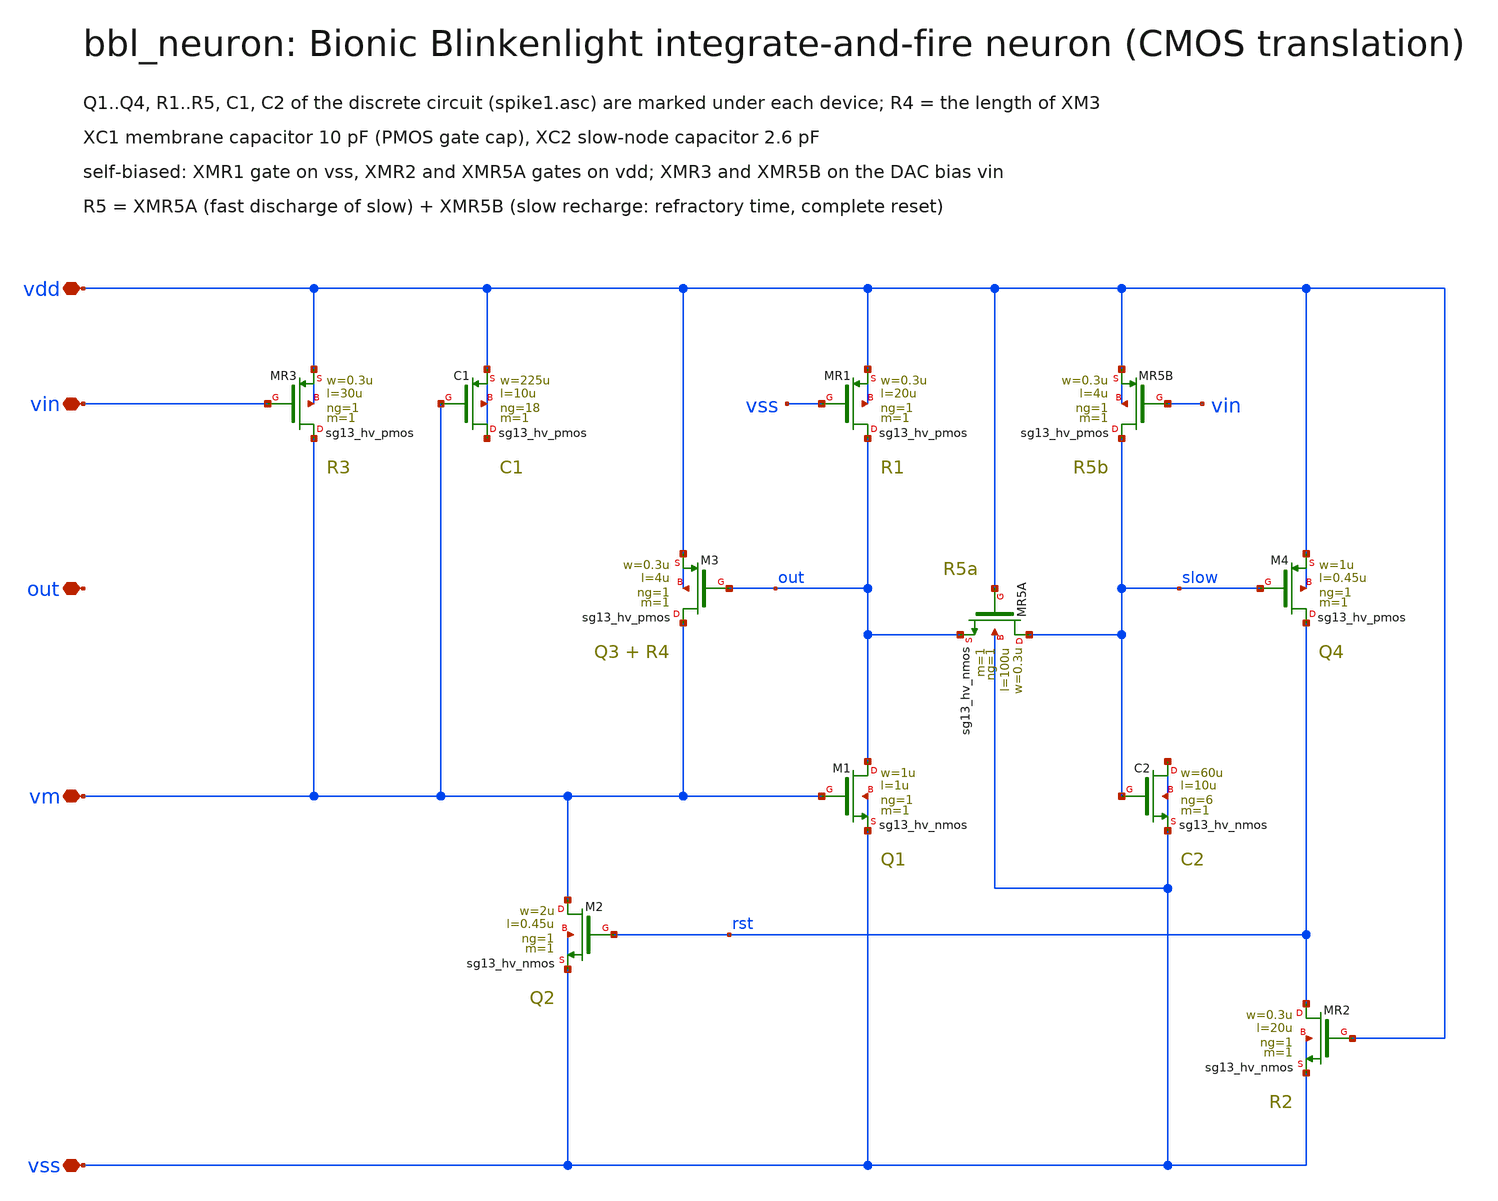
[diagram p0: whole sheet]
** sch_path: schematic/xschem/bbl_neuron.sch
**.subckt bbl_neuron vdd vss vm out vin
*.iopin vdd
*.iopin vss
*.iopin vm
*.iopin out
*.iopin vin
XMR3 vm vin vdd vdd sg13_hv_pmos w=0.3u l=30u ng=1 m=1 mm_ok=1
XC1 vdd vm vdd vdd sg13_hv_pmos w=225u l=10u ng=18 m=1 mm_ok=1
XM2 vm rst vss vss sg13_hv_nmos w=2u l=0.45u ng=1 m=1 mm_ok=1
XM3 vm out vdd vdd sg13_hv_pmos w=0.3u l=4u ng=1 m=1 mm_ok=1
XMR1 out vss vdd vdd sg13_hv_pmos w=0.3u l=20u ng=1 m=1 mm_ok=1
XM1 out vm vss vss sg13_hv_nmos w=1u l=1u ng=1 m=1 mm_ok=1
XMR5A slow vdd out vss sg13_hv_nmos w=0.3u l=100u ng=1 m=1 mm_ok=1
XMR5B slow vin vdd vdd sg13_hv_pmos w=0.3u l=4u ng=1 m=1 mm_ok=1
XC2 vss slow vss vss sg13_hv_nmos w=60u l=10u ng=6 m=1 mm_ok=1
XM4 rst slow vdd vdd sg13_hv_pmos w=1u l=0.45u ng=1 m=1 mm_ok=1
XMR2 rst vdd vss vss sg13_hv_nmos w=0.3u l=20u ng=1 m=1 mm_ok=1
**.ends
.end
